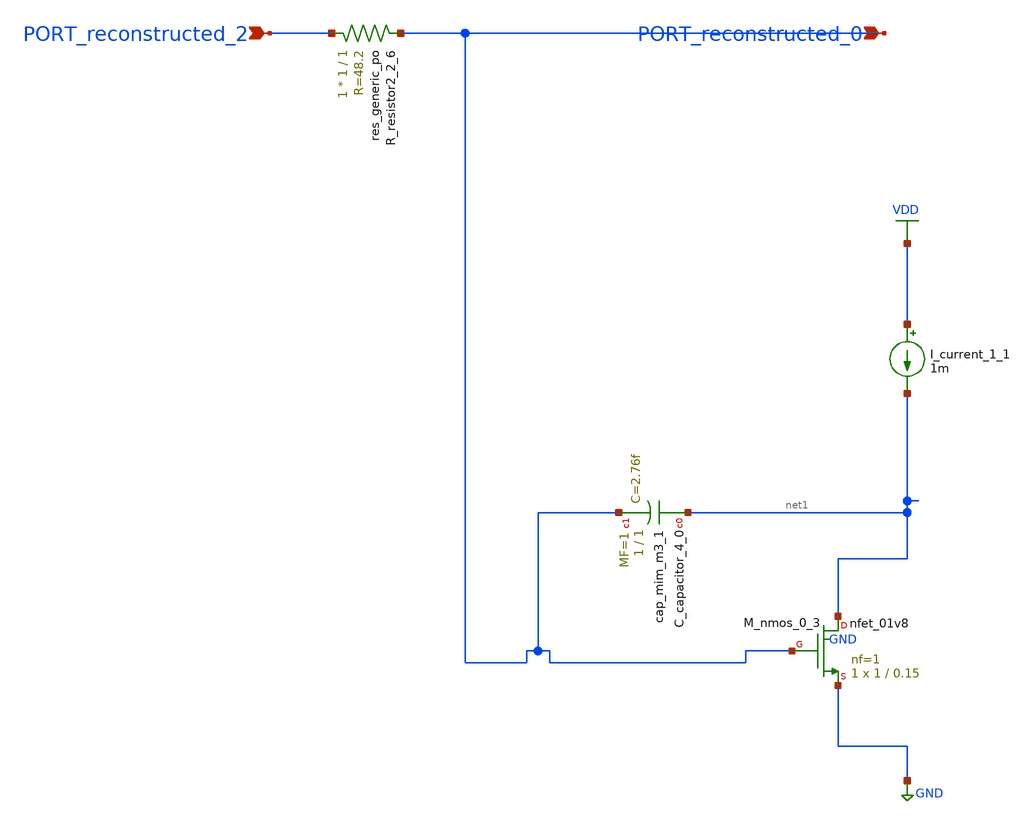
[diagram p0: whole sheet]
** sch_path: schematics/AMSNet/356.sch
**.subckt 356 PORT_reconstructed_2 PORT_reconstructed_0
*.ipin PORT_reconstructed_2
*.ipin PORT_reconstructed_0
XC_capacitor_4_0 net1 PORT_reconstructed_0 sky130_fd_pr__cap_mim_m3_1 W=1 L=1 MF=1 m=1
I_current_1_1 VDD net1 1m
XM_nmos_0_3 net1 PORT_reconstructed_0 GND GND sky130_fd_pr__nfet_01v8 L=0.15 W=1 nf=1 ad='int((1 + 1)/2) * 1 / 1 * 0.29'
+ as='int((1 + 2)/2) * 1 / 1 * 0.29' pd='2*int((1 + 1)/2) * (1 / 1 + 0.29)' ps='2*int((1 + 2)/2) * (1 / 1 + 0.29)'
+ nrd='0.29 / 1 ' nrs='0.29 / 1 ' sa=0 sb=0 sd=0 mult=1 m=1
XR_resistor2_2_6 PORT_reconstructed_2 PORT_reconstructed_0 sky130_fd_pr__res_generic_po W=1 L=1 m=1
**.ends
.GLOBAL GND
.GLOBAL VDD
.end
